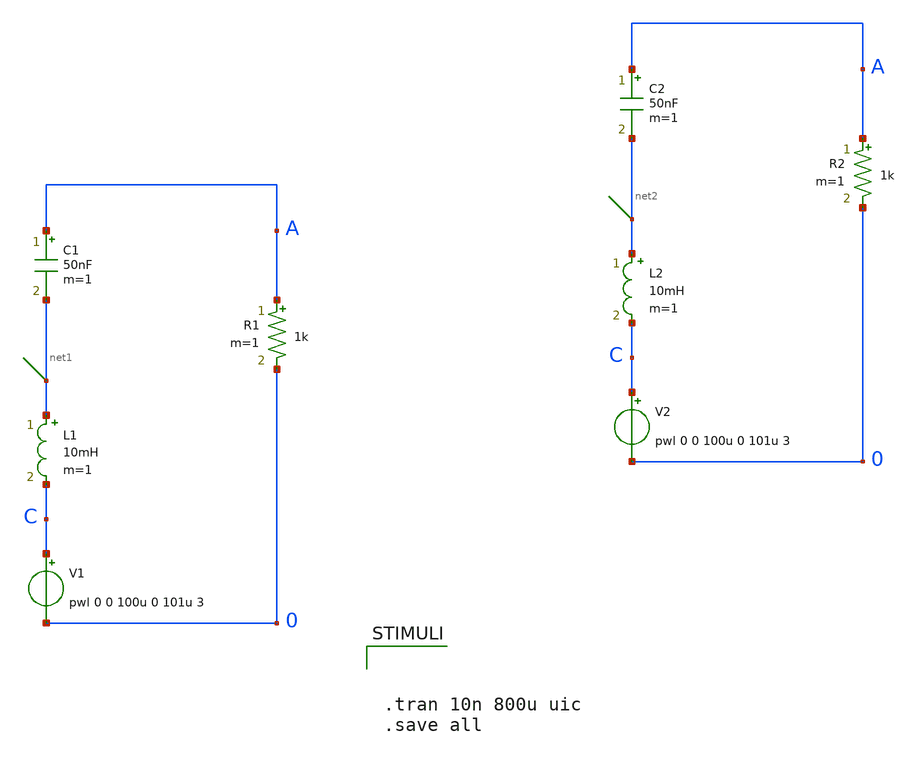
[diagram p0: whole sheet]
** sch_path: xschem_library/examples/rlc.sch
**.subckt rlc
C1 A net1 50nF m=1
R1 A 0 1k m=1
L1 net1 C 10mH m=1
V1 C 0 pwl 0 0 100u 0 101u 3
C2 A net2 50nF m=1
R2 A 0 1k m=1
L2 net2 C 10mH m=1
V2 C 0 pwl 0 0 100u 0 101u 3
**** begin user architecture code



.tran 10n 800u uic
.save all


**** end user architecture code
**.ends
.end
